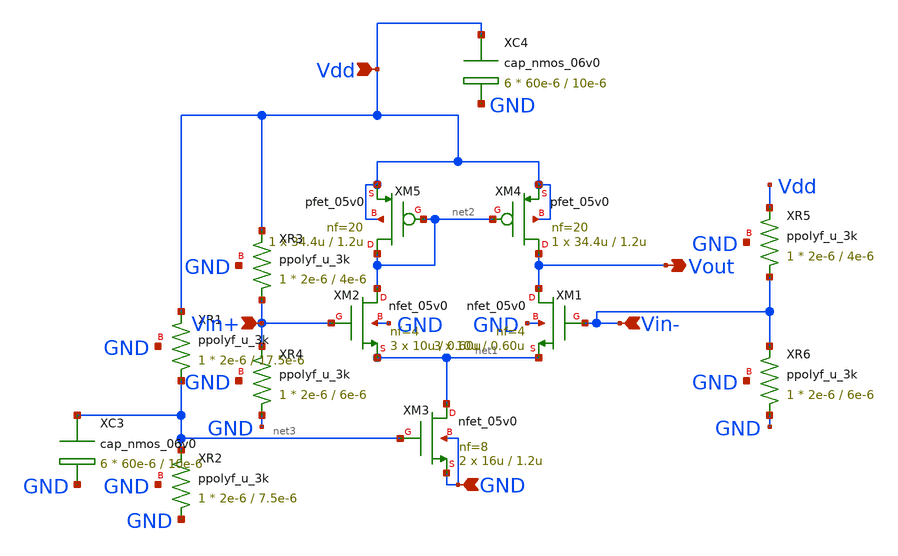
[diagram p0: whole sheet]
** sch_path: RN_Gm3/gm3_makesymbol_old.sch
**.subckt gm3_makesymbol_old Vdd GND Vout Vin+ Vin-
*.ipin Vdd
*.ipin GND
*.opin Vout
*.ipin Vin+
*.ipin Vin-
XM3 net1 net3 GND GND nfet_05v0 L=1.2u W=16u nf=8 ad='int((nf+1)/2) * W/nf * 0.18u' as='int((nf+2)/2) * W/nf * 0.18u'
+ pd='2*int((nf+1)/2) * (W/nf + 0.18u)' ps='2*int((nf+2)/2) * (W/nf + 0.18u)' nrd='0.18u / W' nrs='0.18u / W'
+ sa=0 sb=0 sd=0 m=2
XM4 Vout net2 Vdd Vdd pfet_05v0 L=1.2u W=34.4u nf=20 ad='int((nf+1)/2) * W/nf * 0.18u' as='int((nf+2)/2) * W/nf * 0.18u'
+ pd='2*int((nf+1)/2) * (W/nf + 0.18u)' ps='2*int((nf+2)/2) * (W/nf + 0.18u)' nrd='0.18u / W' nrs='0.18u / W'
+ sa=0 sb=0 sd=0 m=1
XM2 net2 Vin+ net1 GND nfet_05v0 L=0.60u W=10u nf=4 ad='int((nf+1)/2) * W/nf * 0.18u' as='int((nf+2)/2) * W/nf * 0.18u'
+ pd='2*int((nf+1)/2) * (W/nf + 0.18u)' ps='2*int((nf+2)/2) * (W/nf + 0.18u)' nrd='0.18u / W' nrs='0.18u / W'
+ sa=0 sb=0 sd=0 m=3
XM5 net2 net2 Vdd Vdd pfet_05v0 L=1.2u W=34.4u nf=20 ad='int((nf+1)/2) * W/nf * 0.18u' as='int((nf+2)/2) * W/nf * 0.18u'
+ pd='2*int((nf+1)/2) * (W/nf + 0.18u)' ps='2*int((nf+2)/2) * (W/nf + 0.18u)' nrd='0.18u / W' nrs='0.18u / W'
+ sa=0 sb=0 sd=0 m=1
XR1 net3 Vdd GND ppolyf_u_3k r_width=2e-6 r_length=17.5e-6 m=1
XR2 GND net3 GND ppolyf_u_3k r_width=2e-6 r_length=7.5e-6 m=1
XC3 net3 GND cap_nmos_06v0 c_width=60e-6 c_length=10e-6 m=6
XC4 Vdd GND cap_nmos_06v0 c_width=60e-6 c_length=10e-6 m=6
XM1 Vout Vin- net1 GND nfet_05v0 L=0.60u W=10u nf=4 ad='int((nf+1)/2) * W/nf * 0.18u' as='int((nf+2)/2) * W/nf * 0.18u'
+ pd='2*int((nf+1)/2) * (W/nf + 0.18u)' ps='2*int((nf+2)/2) * (W/nf + 0.18u)' nrd='0.18u / W' nrs='0.18u / W'
+ sa=0 sb=0 sd=0 m=3
XR3 Vin+ Vdd GND ppolyf_u_3k r_width=2e-6 r_length=4e-6 m=1
XR4 GND Vin+ GND ppolyf_u_3k r_width=2e-6 r_length=6e-6 m=1
XR5 Vin- Vdd GND ppolyf_u_3k r_width=2e-6 r_length=4e-6 m=1
XR6 GND Vin- GND ppolyf_u_3k r_width=2e-6 r_length=6e-6 m=1
**.ends
.end
